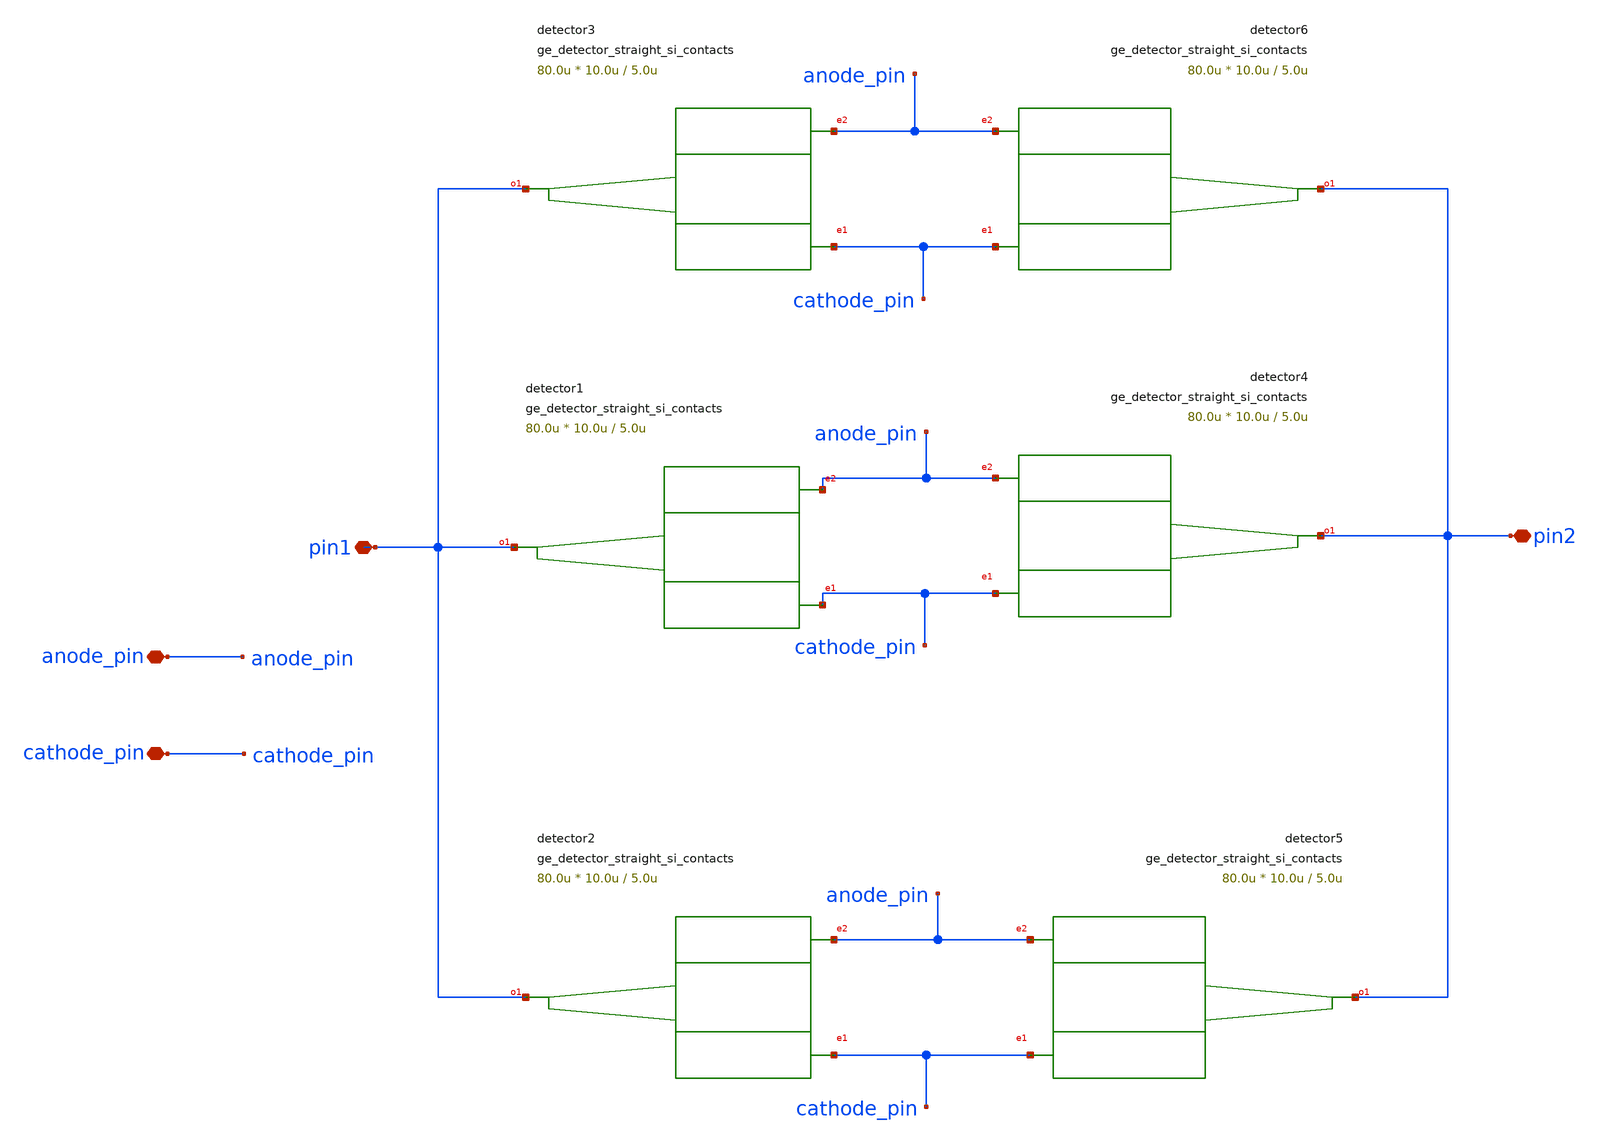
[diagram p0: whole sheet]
** sch_path: xschem/tests/test_sch/test_ge_detector_straight_si_contacts.sch
* Copyright (c) 2024, Mabrains LLC
* Licensed under the GNU Lesser General Public License, Version 3.0 (the "License");
* you may not use this file except in compliance with the License.
* GNU Lesser General Public License
* Version 3, 29 June 2007
* This program is free software: you can redistribute it and/or modify
* it under the terms of the GNU Lesser General Public License as published
* by the Free Software Foundation, either version 3 of the License, or
* (at your option) any later version.
* This program is distributed in the hope that it will be useful,
* but WITHOUT ANY WARRANTY; without even the implied warranty of
* MERCHANTABILITY or FITNESS FOR A PARTICULAR PURPOSE.  See the
* GNU Lesser General Public License for more details.
* You should have received a copy of the GNU Lesser General Public License
* along with this program.  If not, see <https://www.gnu.org/licenses/>.
* SPDX-License-Identifier: LGPL-3.0
**.subckt test_ge_detector_straight_si_contacts cathode_pin anode_pin pin1 pin2
*.iopin cathode_pin
*.iopin anode_pin
*.iopin pin1
*.iopin pin2
Pdetector3 cathode_pin pin1 anode_pin ge_detector_straight_si_contacts length=80.0u
+ via_stack_width=10.0u via_stack_spacing=5.0u via_stack_offset=0.0u
Pdetector1 cathode_pin pin1 anode_pin ge_detector_straight_si_contacts length=80.0u
+ via_stack_width=10.0u via_stack_spacing=5.0u via_stack_offset=0.0u
Pdetector2 cathode_pin pin1 anode_pin ge_detector_straight_si_contacts length=80.0u
+ via_stack_width=10.0u via_stack_spacing=5.0u via_stack_offset=0.0u
Pdetector6 cathode_pin pin2 anode_pin ge_detector_straight_si_contacts length=80.0u
+ via_stack_width=10.0u via_stack_spacing=5.0u via_stack_offset=0.0u
Pdetector4 cathode_pin pin2 anode_pin ge_detector_straight_si_contacts length=80.0u
+ via_stack_width=10.0u via_stack_spacing=5.0u via_stack_offset=0.0u
Pdetector5 cathode_pin pin2 anode_pin ge_detector_straight_si_contacts length=80.0u
+ via_stack_width=10.0u via_stack_spacing=5.0u via_stack_offset=0.0u
**.ends
.end
